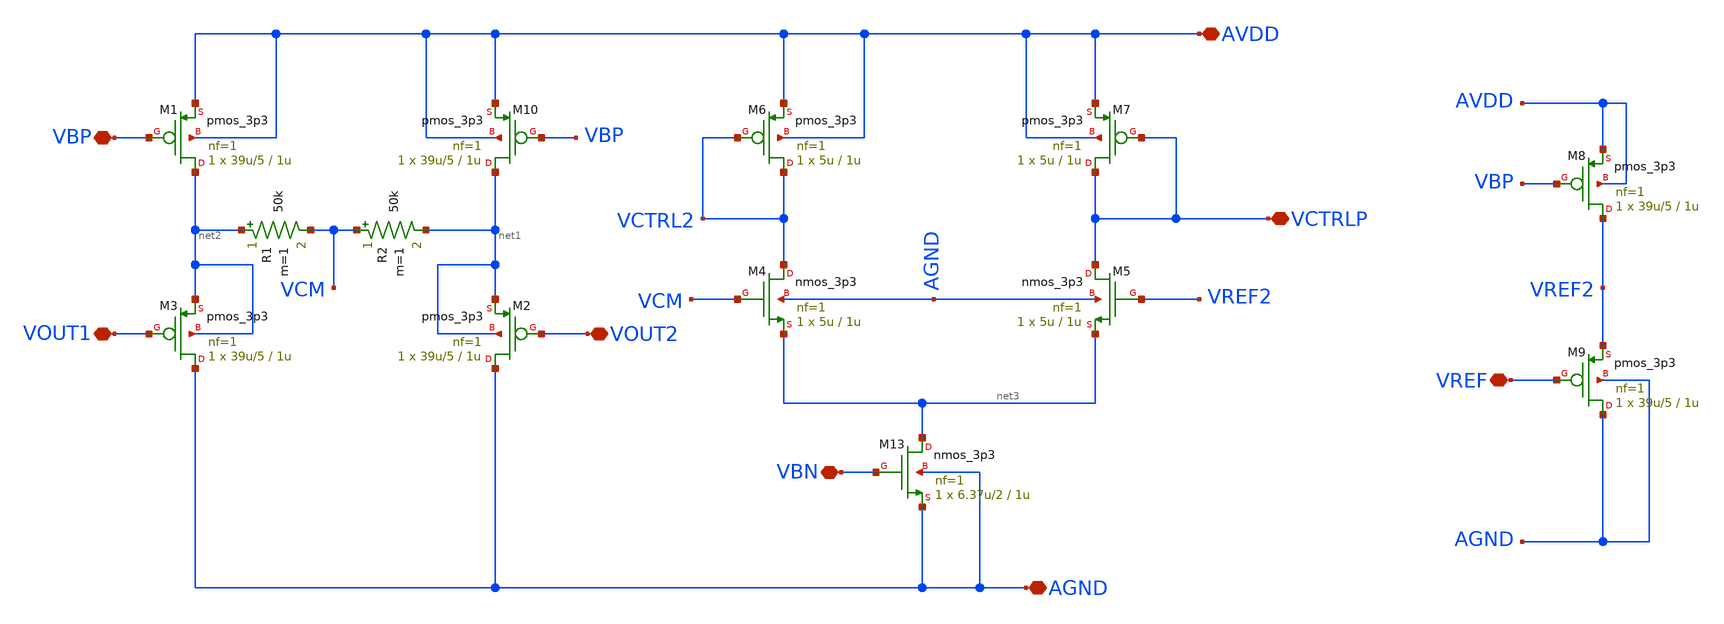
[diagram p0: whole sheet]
** sch_path: ITI_Labs/Lab11_Xschem/Design/CMFB_real.sch
**.subckt CMFB_real VOUT1 VOUT2 VCTRLP VBP AVDD AGND VBN VREF
*.iopin VOUT1
*.iopin VOUT2
*.iopin VCTRLP
*.iopin VBP
*.iopin AVDD
*.iopin AGND
*.iopin VBN
*.iopin VREF
XM4 VCTRL2 VCM net3 AGND nmos_3p3 L=1u W=5u nf=1 ad='int((nf+1)/2) * W/nf * 0.18u' as='int((nf+2)/2) * W/nf * 0.18u'
+ pd='2*int((nf+1)/2) * (W/nf + 0.18u)' ps='2*int((nf+2)/2) * (W/nf + 0.18u)' nrd='0.18u / W' nrs='0.18u / W'
+ sa=0 sb=0 sd=0 m=1
XM5 VCTRLP VREF2 net3 AGND nmos_3p3 L=1u W=5u nf=1 ad='int((nf+1)/2) * W/nf * 0.18u' as='int((nf+2)/2) * W/nf * 0.18u'
+ pd='2*int((nf+1)/2) * (W/nf + 0.18u)' ps='2*int((nf+2)/2) * (W/nf + 0.18u)' nrd='0.18u / W' nrs='0.18u / W'
+ sa=0 sb=0 sd=0 m=1
XM6 VCTRL2 VCTRL2 AVDD AVDD pmos_3p3 L=1u W=5u nf=1 ad='int((nf+1)/2) * W/nf * 0.18u' as='int((nf+2)/2) * W/nf * 0.18u'
+ pd='2*int((nf+1)/2) * (W/nf + 0.18u)' ps='2*int((nf+2)/2) * (W/nf + 0.18u)' nrd='0.18u / W' nrs='0.18u / W'
+ sa=0 sb=0 sd=0 m=1
XM7 VCTRLP VCTRLP AVDD AVDD pmos_3p3 L=1u W=5u nf=1 ad='int((nf+1)/2) * W/nf * 0.18u' as='int((nf+2)/2) * W/nf * 0.18u'
+ pd='2*int((nf+1)/2) * (W/nf + 0.18u)' ps='2*int((nf+2)/2) * (W/nf + 0.18u)' nrd='0.18u / W' nrs='0.18u / W'
+ sa=0 sb=0 sd=0 m=1
R1 net2 VCM 50k m=1
R2 VCM net1 50k m=1
XM10 net1 VBP AVDD AVDD pmos_3p3 L=1u W=39u/5 nf=1 ad='int((nf+1)/2) * W/nf * 0.18u' as='int((nf+2)/2) * W/nf * 0.18u'
+ pd='2*int((nf+1)/2) * (W/nf + 0.18u)' ps='2*int((nf+2)/2) * (W/nf + 0.18u)' nrd='0.18u / W' nrs='0.18u / W'
+ sa=0 sb=0 sd=0 m=1
XM1 net2 VBP AVDD AVDD pmos_3p3 L=1u W=39u/5 nf=1 ad='int((nf+1)/2) * W/nf * 0.18u' as='int((nf+2)/2) * W/nf * 0.18u'
+ pd='2*int((nf+1)/2) * (W/nf + 0.18u)' ps='2*int((nf+2)/2) * (W/nf + 0.18u)' nrd='0.18u / W' nrs='0.18u / W'
+ sa=0 sb=0 sd=0 m=1
XM13 net3 VBN AGND AGND nmos_3p3 L=1u W=6.37u/2 nf=1 ad='int((nf+1)/2) * W/nf * 0.18u' as='int((nf+2)/2) * W/nf * 0.18u'
+ pd='2*int((nf+1)/2) * (W/nf + 0.18u)' ps='2*int((nf+2)/2) * (W/nf + 0.18u)' nrd='0.18u / W' nrs='0.18u / W'
+ sa=0 sb=0 sd=0 m=1
XM2 AGND VOUT2 net1 net1 pmos_3p3 L=1u W=39u/5 nf=1 ad='int((nf+1)/2) * W/nf * 0.18u' as='int((nf+2)/2) * W/nf * 0.18u'
+ pd='2*int((nf+1)/2) * (W/nf + 0.18u)' ps='2*int((nf+2)/2) * (W/nf + 0.18u)' nrd='0.18u / W' nrs='0.18u / W'
+ sa=0 sb=0 sd=0 m=1
XM3 AGND VOUT1 net2 net2 pmos_3p3 L=1u W=39u/5 nf=1 ad='int((nf+1)/2) * W/nf * 0.18u' as='int((nf+2)/2) * W/nf * 0.18u'
+ pd='2*int((nf+1)/2) * (W/nf + 0.18u)' ps='2*int((nf+2)/2) * (W/nf + 0.18u)' nrd='0.18u / W' nrs='0.18u / W'
+ sa=0 sb=0 sd=0 m=1
XM8 VREF2 VBP AVDD AVDD pmos_3p3 L=1u W=39u/5 nf=1 ad='int((nf+1)/2) * W/nf * 0.18u' as='int((nf+2)/2) * W/nf * 0.18u'
+ pd='2*int((nf+1)/2) * (W/nf + 0.18u)' ps='2*int((nf+2)/2) * (W/nf + 0.18u)' nrd='0.18u / W' nrs='0.18u / W'
+ sa=0 sb=0 sd=0 m=1
XM9 AGND VREF VREF2 AGND pmos_3p3 L=1u W=39u/5 nf=1 ad='int((nf+1)/2) * W/nf * 0.18u' as='int((nf+2)/2) * W/nf * 0.18u'
+ pd='2*int((nf+1)/2) * (W/nf + 0.18u)' ps='2*int((nf+2)/2) * (W/nf + 0.18u)' nrd='0.18u / W' nrs='0.18u / W'
+ sa=0 sb=0 sd=0 m=1
**.ends
.end
